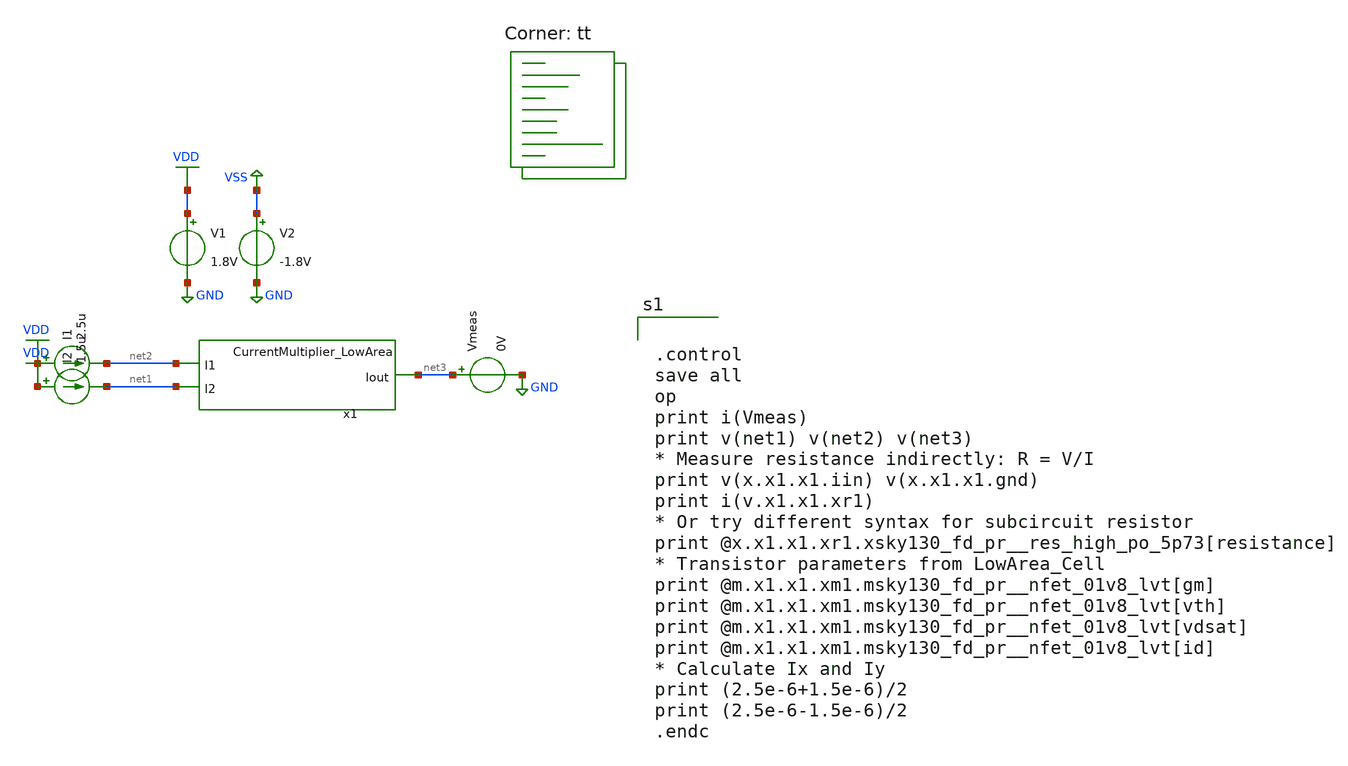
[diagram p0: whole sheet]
** sch_path: analog/library/CurrentMultiplier/testbenches/Functional.sch
**.subckt Functional
x1 net3 net2 net1 CurrentMultiplier_LowArea
I1 VDD net2 2.5u
I2 VDD net1 1.5u
Vmeas net3 GND 0V
V1 VDD GND 1.8V
V2 VSS GND -1.8V
**** begin user architecture code


.control
save all
op
print i(Vmeas)
print v(net1) v(net2) v(net3)
* Measure resistance indirectly: R = V/I
print v(x.x1.x1.iin) v(x.x1.x1.gnd)
print i(v.x1.x1.xr1)
* Or try different syntax for subcircuit resistor
print @x.x1.x1.xr1.xsky130_fd_pr__res_high_po_5p73[resistance]
* Transistor parameters from LowArea_Cell
print @m.x1.x1.xm1.msky130_fd_pr__nfet_01v8_lvt[gm]
print @m.x1.x1.xm1.msky130_fd_pr__nfet_01v8_lvt[vth]
print @m.x1.x1.xm1.msky130_fd_pr__nfet_01v8_lvt[vdsat]
print @m.x1.x1.xm1.msky130_fd_pr__nfet_01v8_lvt[id]
* Calculate Ix and Iy
print (2.5e-6+1.5e-6)/2
print (2.5e-6-1.5e-6)/2
.endc


.lib $::SKYWATER_MODELS/sky130.lib.spice tt
**** end user architecture code
**.ends

* expanding   symbol:  CurrentMultiplier/CurrentMultiplier_LowArea.sym # of pins=3
** sym_path: analog/schematics/components/CurrentMutltiplier/CurrentMultiplier_LowArea.sym
** sch_path: analog/schematics/components/CurrentMutltiplier/CurrentMultiplier_LowArea.sch
.subckt CurrentMultiplier_LowArea Iout I1 I2
*.opin Iout
*.ipin I1
*.ipin I2
x1 I1 Io1 LowArea_Cell
x2 net1 Io1 LowArea_Cell
x3 I2 Iout LowArea_Cell
x4 net2 Iout LowArea_Cell
XM1 Io1 Io1 VDD VDD sky130_fd_pr__pfet_01v8 L=0.15 W=1 nf=1 ad='int((nf+1)/2) * W/nf * 0.29' as='int((nf+2)/2) * W/nf * 0.29'
+ pd='2*int((nf+1)/2) * (W/nf + 0.29)' ps='2*int((nf+2)/2) * (W/nf + 0.29)' nrd='0.29 / W' nrs='0.29 / W'
+ sa=0 sb=0 sd=0 mult=1 m=1
XM2 Iout Io1 VDD VDD sky130_fd_pr__pfet_01v8 L=0.15 W=1 nf=1 ad='int((nf+1)/2) * W/nf * 0.29' as='int((nf+2)/2) * W/nf * 0.29'
+ pd='2*int((nf+1)/2) * (W/nf + 0.29)' ps='2*int((nf+2)/2) * (W/nf + 0.29)' nrd='0.29 / W' nrs='0.29 / W'
+ sa=0 sb=0 sd=0 mult=1 m=1
XM3 net1 I1 GND GND sky130_fd_pr__nfet_01v8 L=0.15 W=1 nf=1 ad='int((nf+1)/2) * W/nf * 0.29' as='int((nf+2)/2) * W/nf * 0.29'
+ pd='2*int((nf+1)/2) * (W/nf + 0.29)' ps='2*int((nf+2)/2) * (W/nf + 0.29)' nrd='0.29 / W' nrs='0.29 / W'
+ sa=0 sb=0 sd=0 mult=1 m=1
XM4 I1 I1 GND GND sky130_fd_pr__nfet_01v8 L=0.15 W=1 nf=1 ad='int((nf+1)/2) * W/nf * 0.29' as='int((nf+2)/2) * W/nf * 0.29'
+ pd='2*int((nf+1)/2) * (W/nf + 0.29)' ps='2*int((nf+2)/2) * (W/nf + 0.29)' nrd='0.29 / W' nrs='0.29 / W'
+ sa=0 sb=0 sd=0 mult=1 m=1
XM5 net2 I2 GND GND sky130_fd_pr__nfet_01v8 L=0.15 W=1 nf=1 ad='int((nf+1)/2) * W/nf * 0.29' as='int((nf+2)/2) * W/nf * 0.29'
+ pd='2*int((nf+1)/2) * (W/nf + 0.29)' ps='2*int((nf+2)/2) * (W/nf + 0.29)' nrd='0.29 / W' nrs='0.29 / W'
+ sa=0 sb=0 sd=0 mult=1 m=1
XM6 I2 I2 GND GND sky130_fd_pr__nfet_01v8 L=0.15 W=1 nf=1 ad='int((nf+1)/2) * W/nf * 0.29' as='int((nf+2)/2) * W/nf * 0.29'
+ pd='2*int((nf+1)/2) * (W/nf + 0.29)' ps='2*int((nf+2)/2) * (W/nf + 0.29)' nrd='0.29 / W' nrs='0.29 / W'
+ sa=0 sb=0 sd=0 mult=1 m=1
.ends


* expanding   symbol:  CurrentMultiplier/LowArea_Cell.sym # of pins=2
** sym_path: analog/schematics/components/LowAreaCell/LowArea_Cell.sym
** sch_path: analog/schematics/components/LowAreaCell/LowArea_Cell.sch
.subckt LowArea_Cell Iout Iin
*.ipin Iin
*.opin Iout
XM1 Iout Iin VSS GND sky130_fd_pr__nfet_01v8_lvt L=0.15 W=1 nf=1 ad='int((nf+1)/2) * W/nf * 0.29' as='int((nf+2)/2) * W/nf * 0.29'
+ pd='2*int((nf+1)/2) * (W/nf + 0.29)' ps='2*int((nf+2)/2) * (W/nf + 0.29)' nrd='0.29 / W' nrs='0.29 / W'
+ sa=0 sb=0 sd=0 mult=1 m=1
XR1 GND Iin GND sky130_fd_pr__res_high_po_5p73 L=11 mult=1 m=1
.ends

.GLOBAL VDD
.GLOBAL VSS
.GLOBAL GND
.end
